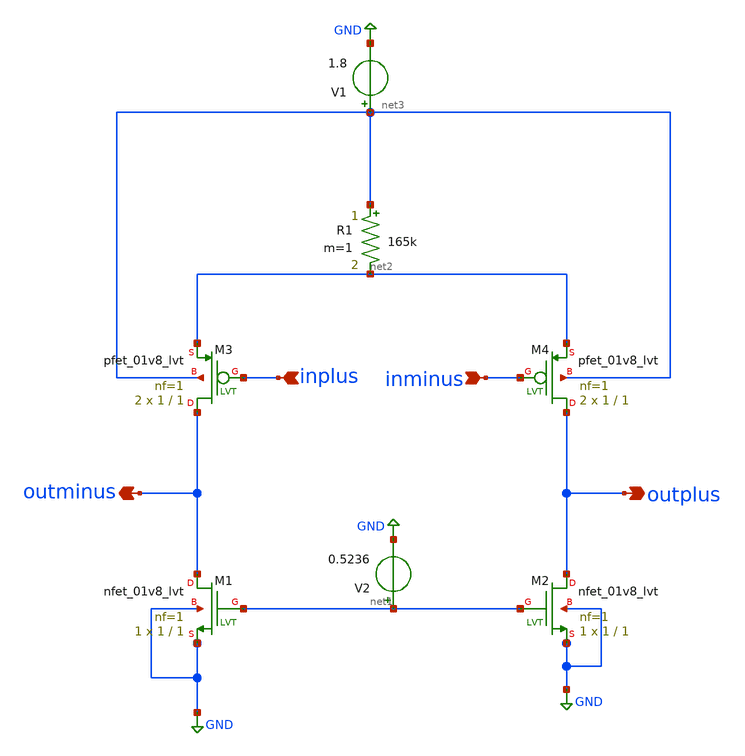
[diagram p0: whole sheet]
** sch_path: topopamp.sch
**.subckt topopamp inplus inminus outplus outminus
*.ipin inplus
*.ipin inminus
*.opin outplus
*.opin outminus
XM1 outminus net1 GND GND sky130_fd_pr__nfet_01v8_lvt L=1 W=1 nf=1 ad='int((nf+1)/2) * W/nf * 0.29' as='int((nf+2)/2) * W/nf * 0.29'
+ pd='2*int((nf+1)/2) * (W/nf + 0.29)' ps='2*int((nf+2)/2) * (W/nf + 0.29)' nrd='0.29 / W' nrs='0.29 / W'
+ sa=0 sb=0 sd=0 mult=1 m=1
XM2 outplus net1 GND GND sky130_fd_pr__nfet_01v8_lvt L=1 W=1 nf=1 ad='int((nf+1)/2) * W/nf * 0.29' as='int((nf+2)/2) * W/nf * 0.29'
+ pd='2*int((nf+1)/2) * (W/nf + 0.29)' ps='2*int((nf+2)/2) * (W/nf + 0.29)' nrd='0.29 / W' nrs='0.29 / W'
+ sa=0 sb=0 sd=0 mult=1 m=1
XM3 outminus inplus net2 net3 sky130_fd_pr__pfet_01v8_lvt L=1 W=1 nf=1 ad='int((nf+1)/2) * W/nf * 0.29'
+ as='int((nf+2)/2) * W/nf * 0.29' pd='2*int((nf+1)/2) * (W/nf + 0.29)' ps='2*int((nf+2)/2) * (W/nf + 0.29)'
+ nrd='0.29 / W' nrs='0.29 / W' sa=0 sb=0 sd=0 mult=2 m=2
XM4 outplus inminus net2 net3 sky130_fd_pr__pfet_01v8_lvt L=1 W=1 nf=1 ad='int((nf+1)/2) * W/nf * 0.29'
+ as='int((nf+2)/2) * W/nf * 0.29' pd='2*int((nf+1)/2) * (W/nf + 0.29)' ps='2*int((nf+2)/2) * (W/nf + 0.29)'
+ nrd='0.29 / W' nrs='0.29 / W' sa=0 sb=0 sd=0 mult=2 m=2
R1 net3 net2 165k m=1
V1 net3 GND 1.8
V2 net1 GND 0.5236
**.ends
.GLOBAL GND
.end
